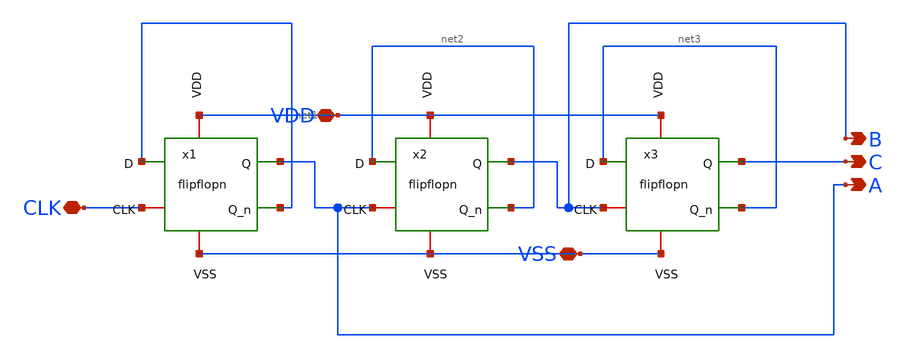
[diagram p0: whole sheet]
** sch_path: netlist/cont3.sch
**.subckt cont3 B CLK VDD VSS C A
*.opin B
*.iopin CLK
*.iopin VDD
*.iopin VSS
*.opin C
*.opin A
x1 CLK net1 VDD A net1 VSS flipflopn
x2 A net2 VDD B net2 VSS flipflopn
x3 B net3 VDD C net3 VSS flipflopn
**.ends
.end
